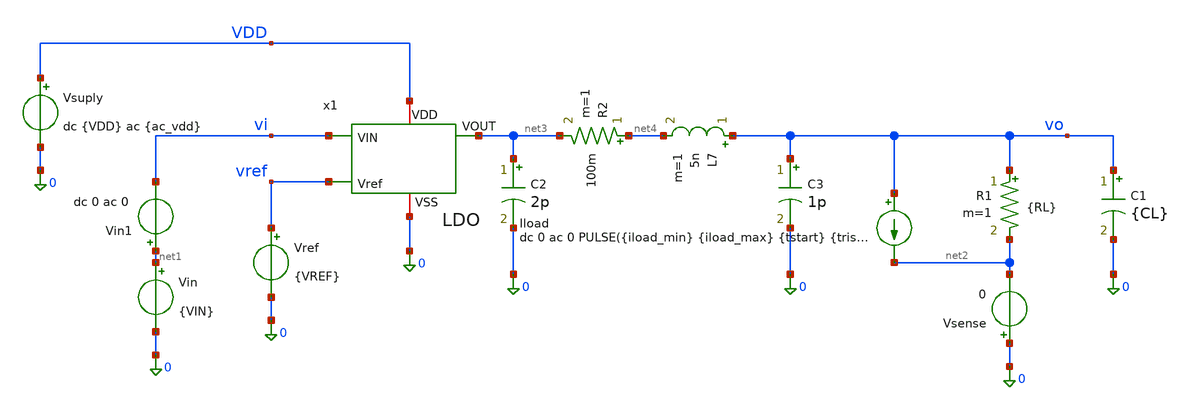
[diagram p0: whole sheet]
** sch_path: xschem/LDO_Top/ldo_tb_montecarlo.sch
**.subckt ldo_tb_montecarlo
Vsuply VDD 0 dc {VDD} ac {ac_vdd}
Vref vref 0 {VREF}
Vin net1 0 {VIN}
Vin1 net1 vi dc 0 ac 0
x1 vi net3 VDD vref 0 LDO
R1 vo net2 {RL} m=1
C1 vo 0 {CL} m=1
Iload vo net2 dc 0 ac 0 PULSE({iload_min} {iload_max} {tstart} {trise} {tfall} {twidth} {tperiod})
Vsense 0 net2 0
C2 net3 0 2p m=1
R2 net4 net3 100m m=1
L7 vo net4 5n m=1
C3 vo 0 1p m=1
**** begin user architecture code






.lib /foss/pdks/sky130A/libs.tech/ngspice/sky130.lib.spice tt_mm
.option temp=27
.option num_threads=8
.param rsh_var = agauss(0, 0.005, 1)

* Forzar un punto de partida para ayudar a la convergencia
.nodeset V(VO)=1.2
.nodeset V(x1.Vre)=0.6


**parametros_ldo
.param VDD = 1.8
.param VREF = 0.6
.param VIN = '1*VDD'
.param RL = 240e9
.param CL = 1u
.param tsim = 2m

* Parámetros para la prueba de carga del LDO
.param iload_min = 1u
.param iload_max = 5m
.param tstart   = 30u
.param trise    = 100n
.param tfall    = 100n
.param twidth   = 100u
.param tperiod  = 200u

.param tsim = '3*tperiod'

.param ac_iprobe = 1
.param ac_vdd = 0




* --- Clamp SOLO de simulación (evita soluciones DC falsas de cientos de V) ---
* Diodo a tierra: conduce si vo baja de -0.2 V
Dclpn 0 vo dclamp_tb
* Diodo a una fuente de 5 V: conduce si vo sube de 5.7 V
Dclpp vo vclp dclamp_tb
* Fuente de referencia para el clamp superior
Dclpn2 0 x1.vre dclamp_tb
Dclpp2 x1.vre vclp dclamp_tb
Vclp vclp 0 5
* Modelo del diodo (fuga ~fA, sin capacitancia: no altera AC ni transitorio)
.model dclamp_tb D(IS=1e-15 N=1)




.control
* =========================================================
* CONFIGURACION DEL BUCLE MONTE CARLO
* =========================================================
let mc_runs = 200
let run = 1

set appendwrite
set filetype=ascii

let tperiod = 200u
let tsim = '3*tperiod'

echo === INICIO MONTE CARLO === > datos_mc.txt

* =========================================================
* INICIO DEL BUCLE
* =========================================================
while run <= mc_runs

    echo ======================================
    echo CORRIENDO MONTE CARLO ITERACION: $&run
    echo ======================================
    echo --- ITERACION: $&run --- >> datos_mc.txt

    * -----------------------------------------------------
    * 1. PREPARAR EL CHIP PARA ESTA ITERACION
    * -----------------------------------------------------
    * Limpiamos memoria y tiramos los dados estadísticos UNA VEZ
    reset

    * Bloqueamos la semilla estadística para que los siguientes 'reset'
    * evalúen exactamente las mismas variaciones físicas (el mismo chip).
    set mc_strict = 1

    * -----------------------------------------------------
    * B. TRANSIENTE (Overshoot y Undershoot)
    * -----------------------------------------------------
    alterparam ac_iprobe = 0
    alterparam ac_vdd = 0
    alterparam RL = 240e9
    reset

    tran 1u $&tsim

    * Acortamos los primeros 150us para evadir el pico del startup
    let t_ignorar = 150u

    meas tran v_estable_ligera FIND v(vo) AT=270u
    meas tran v_estable_pesada FIND v(vo) AT=180u
    meas tran vo_max MAX v(vo) from=$&t_ignorar to=$&tsim
    meas tran vo_min MIN v(vo) from=$&t_ignorar to=$&tsim
    meas tran salida_tran avg v(vo) from=$&t_ignorar to=$&tsim

    let undershoot_mV = (v_estable_ligera - vo_min) * 1e3
    let overshoot_mV = (vo_max - v_estable_pesada) * 1e3

    echo 'undershoot_mV = $&undershoot_mV' >> datos_mc.txt
    echo 'overshoot_mV = $&overshoot_mV' >> datos_mc.txt
    echo 'salida_tran = $&salida_tran' >> datos_mc.txt



    * -----------------------------------------------------
    * C. AC (Estabilidad)
    * -----------------------------------------------------
    alterparam ac_iprobe = 1
    alterparam ac_vdd = 0
    alterparam RL = 240e9
    reset
    alter @Iload[dc] = 10m

    ac dec 10 1 1G
    let T_loop = v(x1.vre) / v(x1.vre2)
    let ldb = vdb(T_loop)
    let fase = vp(T_loop) * 180 / pi

    meas ac ugb WHEN ldb = 0.0
    meas ac fase_ugb FIND fase WHEN ldb = 0.0
    let margen_fase = fase_ugb
    meas ac ganancia_banda_plana find ldb at=1

    echo 'margen_fase = $&margen_fase' >> datos_mc.txt
    echo 'ganancia_banda_plana = $&ganancia_banda_plana' >> datos_mc.txt
    echo 'ugb = $&ugb' >> datos_mc.txt

    * -----------------------------------------------------
    * E. AC (PSRR)
    * -----------------------------------------------------
    alterparam ac_iprobe = 0
    alterparam ac_vdd = 1
    alterparam RL = 240e9
    reset
    alter @Iload[dc] = 10m

    ac dec 10 10 1G
    let psrr1 = v(vdd)/v(vo)
    let psrr_db = vdb(psrr1)

    meas ac gananciaPSRR_1   find psrr_db at=10
    meas ac gananciaPSRR_1k  find psrr_db at=1k
    meas ac gananciaPSRR_10k find psrr_db at=10k
    meas ac gananciaPSRR_1M  find psrr_db at=1Meg

    echo 'psrr_1 = $&gananciaPSRR_1' >> datos_mc.txt
    echo 'psrr_1k = $&gananciaPSRR_1k' >> datos_mc.txt
    echo 'psrr_10k = $&gananciaPSRR_10k' >> datos_mc.txt
    echo 'psrr_1M = $&gananciaPSRR_1M' >> datos_mc.txt

    * -----------------------------------------------------
    * D. TRANSIENTE (Line Regulation)
    * -----------------------------------------------------
    alterparam ac_iprobe = 0
    alterparam ac_vdd = 0
    alterparam RL = 240e9
    reset

    alter @Vin[pwl] = [ 0 1.4 1m 1.8 ]
    alter @Iload[pwl] = [ 0 1u 1m 1u ]

    tran 1u 1m

    let t_line_ini = 40u
    let t_line_fin = 950u

    meas tran voline_max MAX v(vo) from=$&t_line_ini to=$&t_line_fin
    meas tran voline_min MIN v(vo) from=$&t_line_ini to=$&t_line_fin
    meas tran salida_line avg v(vo) from=$&t_line_ini to=$&t_line_fin
    let line_regulation_mV = (voline_max - voline_min)*1000

    echo 'line_regulation_mv = $&line_regulation_mV' >> datos_mc.txt
    echo 'salida_line = $&salida_line' >> datos_mc.txt

    * -----------------------------------------------------
    * F. TRANSIENTE (Load Regulation)
    * -----------------------------------------------------
    reset

    alter @Iload[pwl] = [ 0 1u 1m 5m ]
    alterparam RL = 240e9

    tran 1u 1m

    meas tran vout_light FIND v(vo) AT=40u
    meas tran vout_heavy FIND v(vo) AT=1m

    let load_regulation_mV = (vout_light - vout_heavy) * 1000

    echo 'load_regulation_mV = $&load_regulation_mV' >> datos_mc.txt

    * -----------------------------------------------------
    * G. TRANSIENTE (Dropout)
    * -----------------------------------------------------
    alterparam RL = 240
    reset

    alter @Vin[pwl] = [ 0 2 1m 0 ]
    alter @Iload[pwl] = [ 0 1u 1m 1u ]

    tran 1u 1m

    meas tran vout_nom FIND v(vo) AT=225u
    let vout_target = vout_nom * 0.95

    meas tran vin_do FIND v(vi) WHEN v(vo) = vout_target fall=1
    let dropout_mV = (vin_do - vout_target) * 1e3

    echo 'dropout_mV = $&dropout_mV' >> datos_mc.txt

    * -----------------------------------------------------
    * IMPORTANTE: Desbloquear la semilla para la siguiente iteración
    * -----------------------------------------------------
    unset mc_strict

    let run = run + 1
end

echo === FIN MONTE CARLO === >> datos_mc.txt
echo ======================================
echo SIMULACION MONTE CARLO FINALIZADA
echo ======================================
.endc









**** end user architecture code
**.ends
.end
